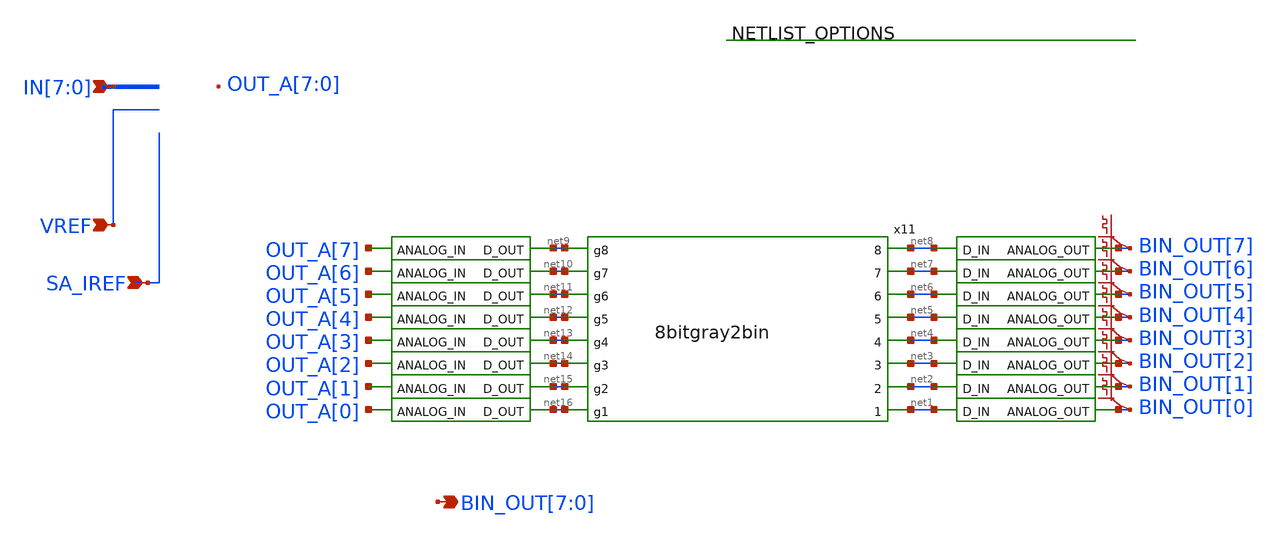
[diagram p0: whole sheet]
** sch_path: xschem/post_layout/8bit_SA_conv_layout.sch
**.subckt 8bit_SA_conv_layout IN[7],IN[6],IN[5],IN[4],IN[3],IN[2],IN[1],IN[0] VREF
*+ BIN_OUT[7],BIN_OUT[6],BIN_OUT[5],BIN_OUT[4],BIN_OUT[3],BIN_OUT[2],BIN_OUT[1],BIN_OUT[0] SA_IREF
*.ipin IN[7],IN[6],IN[5],IN[4],IN[3],IN[2],IN[1],IN[0]
*.ipin VREF
*.opin BIN_OUT[7],BIN_OUT[6],BIN_OUT[5],BIN_OUT[4],BIN_OUT[3],BIN_OUT[2],BIN_OUT[1],BIN_OUT[0]
*.ipin SA_IREF
x11 net8 net9 net10 net7 net6 net11 net5 net12 net13 net4 net3 net14 net15 net2 net16 net1
+ 8bitgray2bin
x12 BIN_OUT[7] net8 dac_bridge
x13 BIN_OUT[6] net7 dac_bridge
x14 BIN_OUT[5] net6 dac_bridge
x16 BIN_OUT[4] net5 dac_bridge
x17 BIN_OUT[3] net4 dac_bridge
x18 BIN_OUT[2] net3 dac_bridge
x19 BIN_OUT[1] net2 dac_bridge
x37 BIN_OUT[0] net1 dac_bridge
x39 net9 OUT_A[7] adc_bridge
x40 net10 OUT_A[6] adc_bridge
x41 net11 OUT_A[5] adc_bridge
x42 net12 OUT_A[4] adc_bridge
x43 net13 OUT_A[3] adc_bridge
x44 net14 OUT_A[2] adc_bridge
x45 net15 OUT_A[1] adc_bridge
x46 net16 OUT_A[0] adc_bridge
.save v(bin_out[7])
.save v(bin_out[6])
.save v(bin_out[5])
.save v(bin_out[4])
.save v(bin_out[3])
.save v(bin_out[2])
.save v(bin_out[1])
.save v(bin_out[0])
**.ends

* expanding   symbol:  adc/8bitgray2bin.sym # of pins=16
** sym_path: xschem/adc/8bitgray2bin.sym
** sch_path: xschem/adc/8bitgray2bin.sch
.subckt 8bitgray2bin 8 g8 g7 7 6 g6 5 g5 g4 4 3 g3 g2 2 g1 1
*.opin 7
*.opin 6
*.opin 5
*.opin 4
*.opin 3
*.opin 2
*.opin 1
*.opin 8
*.ipin g5
*.ipin g4
*.ipin g3
*.ipin g8
*.ipin g7
*.ipin g6
*.ipin g2
*.ipin g1
**** begin user architecture code


* lsb first.
a1 [g1 g2 g3 g4 g5 g6 g7 g8] [1 2 3 4 5 6 7 8] gray2bin_lut
.model gray2bin_lut d_genlut(rise_delay=[1p 1p] fall_delay=[1p 1p]  input_load=[1p 1p]
+ input_delay=[0 0]
+ table_values=01101001100101101001011001101001100101100110100101101001100101101001011001101001011010011001011001101001100101101001011001101001100101100110100101101001100101100110100110010110100101100110100101101001100101101001011001101001100101100110100101101001100101100011110011000011110000110011110011000011001111000011110011000011110000110011110000111100110000110011110011000011110000110011110011000011001111000011110011000011001111001100001111000011001111000011110011000011110000110011110011000011001111000011110011000011000011111111000011110000000011111111000000001111000011111111000011110000000011110000111111110000000011111111000011110000000011111111000000001111000011111111000000001111111100001111000000001111000011111111000011110000000011111111000000001111000011111111000000000000111111111111111100000000111111110000000000000000111111111111111100000000000000001111111100000000111111111111111100000000111111110000000000000000111111110000000011111111111111110000000000000000111111111111111100000000111111110000000000000000111111110000000000000000111111111111111111111111111111110000000000000000111111111111111100000000000000000000000000000000111111111111111111111111111111110000000000000000000000000000000011111111111111110000000000000000111111111111111111111111111111110000000000000000000000000000000000000000000000001111111111111111111111111111111111111111111111111111111111111111000000000000000000000000000000001111111111111111111111111111111100000000000000000000000000000000000000000000000000000000000000001111111111111111111111111111111100000000000000000000000000000000000000000000000000000000000000001111111111111111111111111111111111111111111111111111111111111111111111111111111111111111111111111111111111111111111111111111111100000000000000000000000000000000000000000000000000000000000000000000000000000000000000000000000000000000000000000000000000000000000000000000000000000000000000000000000000000000000000000000000011111111111111111111111111111111111111111111111111111111111111111111111111111111111111111111111111111111111111111111111111111111)




**** end user architecture code
.ends


* expanding   symbol:  digital_prims/dac_bridge.sym # of pins=2
** sym_path: xschem/digital_prims/dac_bridge.sym
** sch_path: xschem/digital_prims/dac_bridge.sch
.subckt dac_bridge ANALOG_OUT D_IN
*.ipin D_IN
*.opin ANALOG_OUT
**** begin user architecture code


abridge_d [D_IN] [ANALOG_OUT] dac_buff
.model dac_buff dac_bridge(out_high=1.8)


**** end user architecture code
.ends


* expanding   symbol:  digital_prims/adc_bridge.sym # of pins=2
** sym_path: xschem/digital_prims/adc_bridge.sym
** sch_path: xschem/digital_prims/adc_bridge.sch
.subckt adc_bridge D_OUT ANALOG_IN
*.ipin ANALOG_IN
*.opin D_OUT
**** begin user architecture code


abridge [ANALOG_IN] [D_OUT] adc_buff
.model adc_buff adc_bridge(in_low=0.9 in_high =0.9)


**** end user architecture code
.ends

**** begin user architecture code


Xsens_amp_2 INx5x SA_IREF OUT_Ax5x VREF VDD GND sens_amp
Xsens_amp_3 INx4x SA_IREF OUT_Ax4x VREF VDD GND sens_amp
Xsens_amp_4 INx3x SA_IREF OUT_Ax3x VREF VDD GND sens_amp
Xsens_amp_5 INx2x SA_IREF OUT_Ax2x VREF VDD GND sens_amp
Xsens_amp_6 INx1x SA_IREF OUT_Ax1x VREF VDD GND sens_amp
Xsens_amp_7 INx0x SA_IREF OUT_Ax0x VREF VDD GND sens_amp
Xsens_amp_0 INx7x SA_IREF OUT_Ax7x VREF VDD GND sens_amp
Xsens_amp_1 INx6x SA_IREF OUT_Ax6x VREF VDD GND sens_amp


.subckt sens_amp V_IN SA_IREF OUT REF VDD GND
X0 GN GN VDD VDD sky130_fd_pr__pfet_01v8_lvt ad=3.5e+11p pd=2.7e+06u as=1.8e+12p ps=1.22e+07u
+ w=1e+06u l=500000u
X1 net1 V_IN net2 GND sky130_fd_pr__nfet_01v8_lvt ad=1.4e+12p pd=8.7e+06u as=1.775e+12p ps=1.05e+07u
+ w=4e+06u l=150000u
X2 net2 REF GN GND sky130_fd_pr__nfet_01v8_lvt ad=0p pd=0u as=1.45e+12p ps=9.1e+06u w=4e+06u
+ l=150000u
X3 net1 GN VDD VDD sky130_fd_pr__pfet_01v8_lvt ad=3.5e+11p pd=2.7e+06u as=0p ps=0u w=1e+06u
+ l=500000u
X4 net2 SA_IREF GND GND sky130_fd_pr__nfet_01v8_lvt ad=0p pd=0u as=6e+11p ps=4.7e+06u w=500000u
+ l=1e+06u
X5 OUT net1 VDD VDD sky130_fd_pr__pfet_01v8_lvt ad=1.05e+12p pd=6.7e+06u as=0p ps=0u w=3e+06u
+ l=350000u
X6 OUT net1 GND GND sky130_fd_pr__nfet_01v8_lvt ad=3.5e+11p pd=2.7e+06u as=0p ps=0u w=1e+06u
+ l=150000u
.ends




**** end user architecture code
.end
